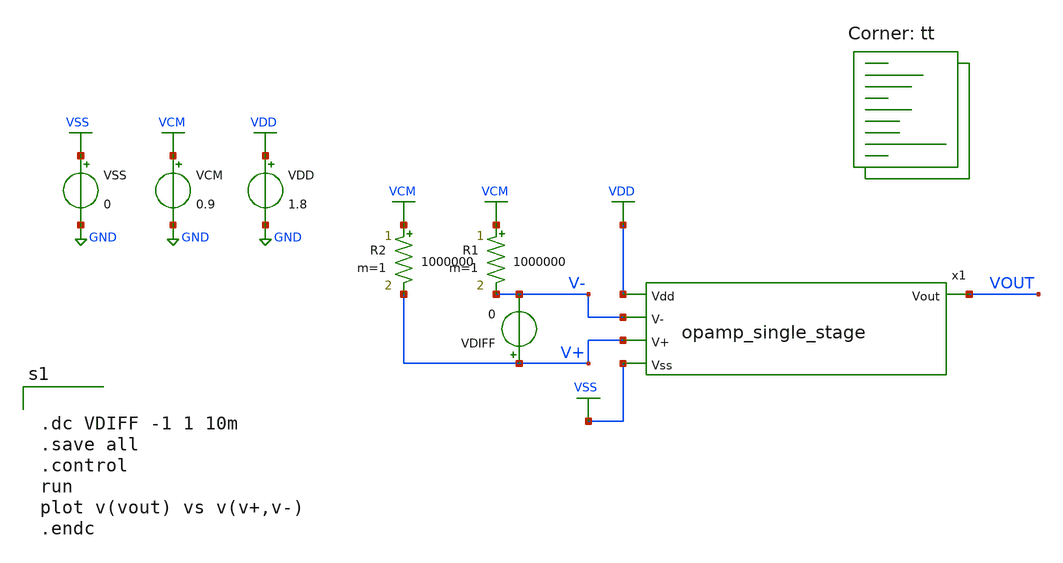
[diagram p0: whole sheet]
** sch_path: analog/schematics/tb_dc_analysis.sch
**.subckt tb_dc_analysis
VDD VDD GND 1.8
VCM VCM GND 0.9
R1 VCM V- 1000000 m=1
R2 VCM V+ 1000000 m=1
VSS VSS GND 0
VDIFF V+ V- 0
x1 VDD V- V+ VOUT VSS opamp_single_stage
**** begin user architecture code


.dc VDIFF -1 1 10m
.save all
.control
run
plot v(vout) vs v(v+,v-)
.endc


.lib $::SKYWATER_MODELS/sky130.lib.spice tt
**** end user architecture code
**.ends

* expanding   symbol:  opamp_single_stage.sym # of pins=5
** sym_path: analog/schematics/opamp_single_stage.sym
** sch_path: analog/schematics/opamp_single_stage.sch
.subckt opamp_single_stage Vdd V- V+ Vout Vss
*.opin Vout
*.ipin Vdd
*.ipin Vss
*.ipin V+
*.ipin V-
XM3 net1 V- net3 Vss sky130_fd_pr__nfet_01v8 L=0.6 W=10 nf=1 ad='int((nf+1)/2) * W/nf * 0.29' as='int((nf+2)/2) * W/nf * 0.29'
+ pd='2*int((nf+1)/2) * (W/nf + 0.29)' ps='2*int((nf+2)/2) * (W/nf + 0.29)' nrd='0.29 / W' nrs='0.29 / W'
+ sa=0 sb=0 sd=0 mult=1 m=1
XM4 net2 V+ net3 Vss sky130_fd_pr__nfet_01v8 L=0.6 W=10 nf=1 ad='int((nf+1)/2) * W/nf * 0.29' as='int((nf+2)/2) * W/nf * 0.29'
+ pd='2*int((nf+1)/2) * (W/nf + 0.29)' ps='2*int((nf+2)/2) * (W/nf + 0.29)' nrd='0.29 / W' nrs='0.29 / W'
+ sa=0 sb=0 sd=0 mult=1 m=1
XM5 net3 net4 Vss Vss sky130_fd_pr__nfet_01v8 L=0.15 W=8 nf=1 ad='int((nf+1)/2) * W/nf * 0.29' as='int((nf+2)/2) * W/nf * 0.29'
+ pd='2*int((nf+1)/2) * (W/nf + 0.29)' ps='2*int((nf+2)/2) * (W/nf + 0.29)' nrd='0.29 / W' nrs='0.29 / W'
+ sa=0 sb=0 sd=0 mult=1 m=1
XM1 net1 net1 Vdd Vdd sky130_fd_pr__pfet_01v8 L=1 W=6 nf=1 ad='int((nf+1)/2) * W/nf * 0.29' as='int((nf+2)/2) * W/nf * 0.29'
+ pd='2*int((nf+1)/2) * (W/nf + 0.29)' ps='2*int((nf+2)/2) * (W/nf + 0.29)' nrd='0.29 / W' nrs='0.29 / W'
+ sa=0 sb=0 sd=0 mult=1 m=1
XM2 net2 net1 Vdd Vdd sky130_fd_pr__pfet_01v8 L=1 W=6 nf=1 ad='int((nf+1)/2) * W/nf * 0.29' as='int((nf+2)/2) * W/nf * 0.29'
+ pd='2*int((nf+1)/2) * (W/nf + 0.29)' ps='2*int((nf+2)/2) * (W/nf + 0.29)' nrd='0.29 / W' nrs='0.29 / W'
+ sa=0 sb=0 sd=0 mult=1 m=1
XM6 net4 net4 Vss Vss sky130_fd_pr__nfet_01v8 L=0.15 W=8 nf=1 ad='int((nf+1)/2) * W/nf * 0.29' as='int((nf+2)/2) * W/nf * 0.29'
+ pd='2*int((nf+1)/2) * (W/nf + 0.29)' ps='2*int((nf+2)/2) * (W/nf + 0.29)' nrd='0.29 / W' nrs='0.29 / W'
+ sa=0 sb=0 sd=0 mult=1 m=1
XM8 Vout net4 Vss Vss sky130_fd_pr__nfet_01v8 L=0.15 W=8 nf=1 ad='int((nf+1)/2) * W/nf * 0.29' as='int((nf+2)/2) * W/nf * 0.29'
+ pd='2*int((nf+1)/2) * (W/nf + 0.29)' ps='2*int((nf+2)/2) * (W/nf + 0.29)' nrd='0.29 / W' nrs='0.29 / W'
+ sa=0 sb=0 sd=0 mult=1 m=1
XM7 Vout net2 Vdd Vdd sky130_fd_pr__pfet_01v8 L=1 W=6 nf=1 ad='int((nf+1)/2) * W/nf * 0.29' as='int((nf+2)/2) * W/nf * 0.29'
+ pd='2*int((nf+1)/2) * (W/nf + 0.29)' ps='2*int((nf+2)/2) * (W/nf + 0.29)' nrd='0.29 / W' nrs='0.29 / W'
+ sa=0 sb=0 sd=0 mult=1 m=1
XR1 net4 Vdd net5 sky130_fd_pr__res_high_po_5p73 L=5 mult=1 m=1
.ends

.GLOBAL GND
.GLOBAL VDD
.GLOBAL VCM
.GLOBAL VSS
.end
